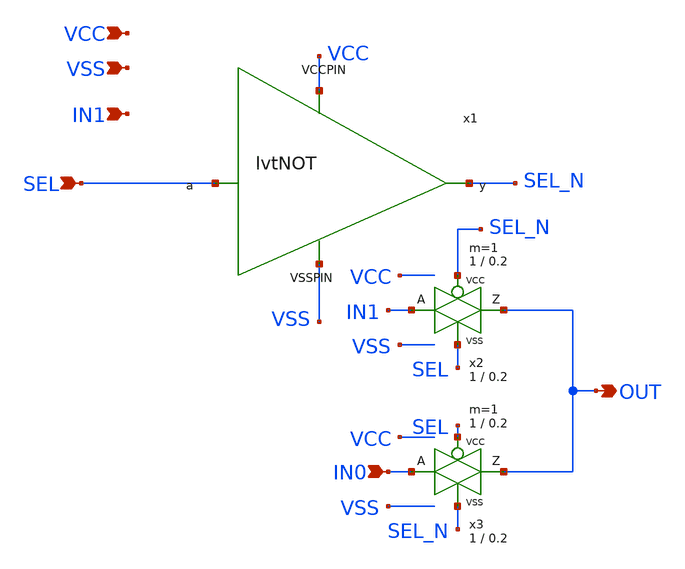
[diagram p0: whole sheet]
** sch_path: onehot2mux.sch
**.subckt onehot2mux SEL IN0 OUT VCC VSS IN1
*.ipin SEL
*.ipin IN0
*.opin OUT
*.ipin VCC
*.ipin VSS
*.ipin IN1
x2 OUT IN1 SEL_N SEL VCC VSS passgate W_N=1 L_N=0.2 W_P=1 L_P=0.2 m=1
x3 OUT IN0 SEL SEL_N VCC VSS passgate W_N=1 L_N=0.2 W_P=1 L_P=0.2 m=1
x1 VSS VCC SEL SEL_N lvtNOT
**.ends

* expanding   symbol:  passgate.sym # of pins=4
** sym_path: passgate.sym
** sch_path: passgate.sch
.subckt passgate Z A GP GN VCCBPIN VSSBPIN  W_N=1 L_N=0.2 W_P=1 L_P=0.2

*.iopin A
*.iopin Z
*.ipin GP
*.ipin GN
XM1 A GN Z VSS sky130_fd_pr__nfet_01v8 W=W_N L=L_N ad='W * 0.29' pd='W + 2 * 0.29' as='W * 0.29' ps='W + 2 * 0.29'
+ nrd=0 nrs=0 sa=0 sb=0 sd=0 nf=1 mult=1
XM2 A GP Z VCC sky130_fd_pr__pfet_01v8 W=W_P L=L_P ad='W * 0.29' pd='W + 2 * 0.29' as='W * 0.29' ps='W + 2 * 0.29'
+ nrd=0 nrs=0 sa=0 sb=0 sd=0 nf=1 mult=1
.ends


* expanding   symbol:  /home/ttuser/Documents/ADCAnalogDesign/lvtNOT.sym # of pins=4
** sym_path: lvtNOT.sym
** sch_path: lvtNOT.sch
.subckt lvtNOT VSSPIN VCCPIN a y
*.ipin a
*.opin y
*.ipin VSSPIN
*.ipin VCCPIN
XM2 y a VCCPIN VCCPIN sky130_fd_pr__pfet_01v8_lvt L=0.35 W=2 nf=1 ad='int((1 + 1)/2) * 2 / 1 * 0.29'
+ as='int((1 + 2)/2) * 2 / 1 * 0.29' pd='2*int((1 + 1)/2) * (2 / 1 + 0.29)' ps='2*int((1 + 2)/2) * (2 / 1 + 0.29)'
+ nrd='0.29 / 2 ' nrs='0.29 / 2 ' sa=0 sb=0 sd=0 mult=1 m=1
XM1 y a VSSPIN VSSPIN sky130_fd_pr__nfet_01v8_lvt L=0.15 W=1 nf=1 ad='int((nf+1)/2) * W/nf * 0.29' as='int((nf+2)/2) * W/nf * 0.29'
+ pd='2*int((nf+1)/2) * (W/nf + 0.29)' ps='2*int((nf+2)/2) * (W/nf + 0.29)' nrd='0.29 / W' nrs='0.29 / W'
+ sa=0 sb=0 sd=0 mult=1 m=1
.ends

.end
